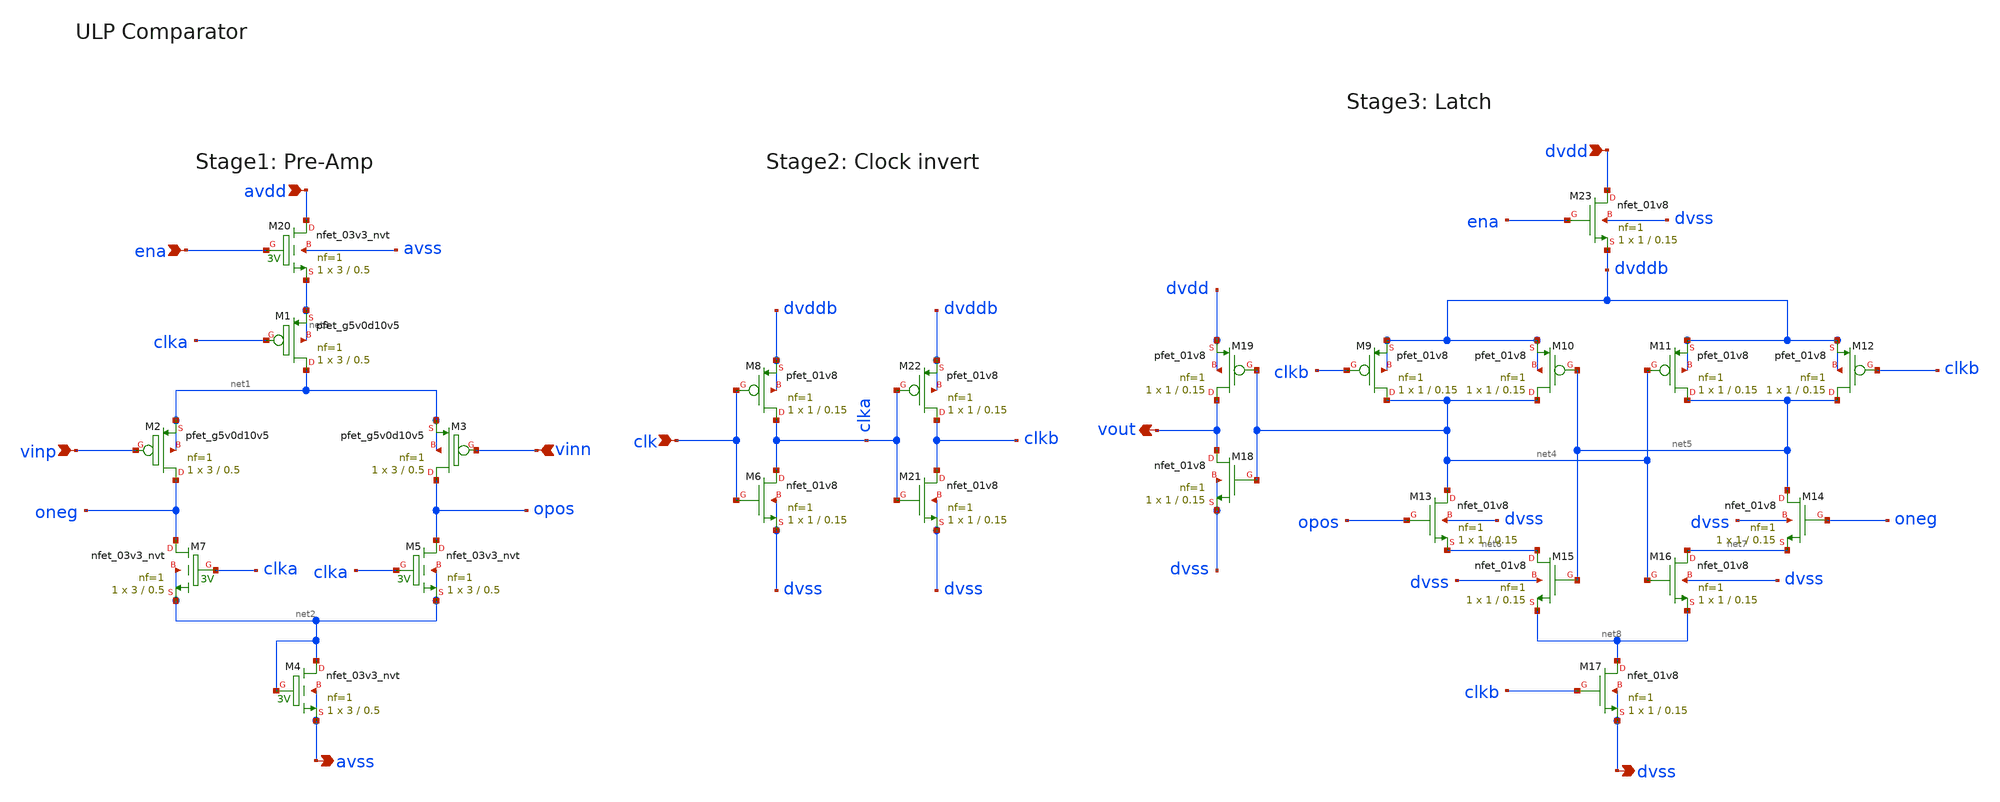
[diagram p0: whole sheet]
** sch_path: xschem/sky130_icrg_ip__ulpcomp2.sch
**.subckt sky130_icrg_ip__ulpcomp2 avdd vinp vinn avss vout dvss dvdd clk ena
*.ipin avdd
*.ipin vinp
*.ipin vinn
*.opin avss
*.opin vout
*.opin dvss
*.ipin dvdd
*.ipin clk
*.ipin ena
XM1 net1 clka net3 net3 sky130_fd_pr__pfet_g5v0d10v5 L=0.5 W=3 nf=1 ad='int((nf+1)/2) * W/nf * 0.29'
+ as='int((nf+2)/2) * W/nf * 0.29' pd='2*int((nf+1)/2) * (W/nf + 0.29)' ps='2*int((nf+2)/2) * (W/nf + 0.29)'
+ nrd='0.29 / W' nrs='0.29 / W' sa=0 sb=0 sd=0 mult=1 m=1
XM2 oneg vinp net1 net1 sky130_fd_pr__pfet_g5v0d10v5 L=0.5 W=3 nf=1 ad='int((nf+1)/2) * W/nf * 0.29'
+ as='int((nf+2)/2) * W/nf * 0.29' pd='2*int((nf+1)/2) * (W/nf + 0.29)' ps='2*int((nf+2)/2) * (W/nf + 0.29)'
+ nrd='0.29 / W' nrs='0.29 / W' sa=0 sb=0 sd=0 mult=1 m=1
XM3 opos vinn net1 net1 sky130_fd_pr__pfet_g5v0d10v5 L=0.5 W=3 nf=1 ad='int((nf+1)/2) * W/nf * 0.29'
+ as='int((nf+2)/2) * W/nf * 0.29' pd='2*int((nf+1)/2) * (W/nf + 0.29)' ps='2*int((nf+2)/2) * (W/nf + 0.29)'
+ nrd='0.29 / W' nrs='0.29 / W' sa=0 sb=0 sd=0 mult=1 m=1
XM7 oneg clka net2 net2 sky130_fd_pr__nfet_03v3_nvt L=0.5 W=3 nf=1 ad='int((nf+1)/2) * W/nf * 0.29' as='int((nf+2)/2) * W/nf * 0.29'
+ pd='2*int((nf+1)/2) * (W/nf + 0.29)' ps='2*int((nf+2)/2) * (W/nf + 0.29)' nrd='0.29 / W' nrs='0.29 / W'
+ sa=0 sb=0 sd=0 mult=1 m=1
XM5 opos clka net2 net2 sky130_fd_pr__nfet_03v3_nvt L=0.5 W=3 nf=1 ad='int((nf+1)/2) * W/nf * 0.29' as='int((nf+2)/2) * W/nf * 0.29'
+ pd='2*int((nf+1)/2) * (W/nf + 0.29)' ps='2*int((nf+2)/2) * (W/nf + 0.29)' nrd='0.29 / W' nrs='0.29 / W'
+ sa=0 sb=0 sd=0 mult=1 m=1
XM6 clka clk dvss dvss sky130_fd_pr__nfet_01v8 L=0.15 W=1 nf=1 ad='int((nf+1)/2) * W/nf * 0.29' as='int((nf+2)/2) * W/nf * 0.29'
+ pd='2*int((nf+1)/2) * (W/nf + 0.29)' ps='2*int((nf+2)/2) * (W/nf + 0.29)' nrd='0.29 / W' nrs='0.29 / W'
+ sa=0 sb=0 sd=0 mult=1 m=1
XM8 clka clk dvddb dvddb sky130_fd_pr__pfet_01v8 L=0.15 W=1 nf=1 ad='int((nf+1)/2) * W/nf * 0.29' as='int((nf+2)/2) * W/nf * 0.29'
+ pd='2*int((nf+1)/2) * (W/nf + 0.29)' ps='2*int((nf+2)/2) * (W/nf + 0.29)' nrd='0.29 / W' nrs='0.29 / W'
+ sa=0 sb=0 sd=0 mult=1 m=1
XM9 net4 clkb dvddb dvddb sky130_fd_pr__pfet_01v8 L=0.15 W=1 nf=1 ad='int((nf+1)/2) * W/nf * 0.29' as='int((nf+2)/2) * W/nf * 0.29'
+ pd='2*int((nf+1)/2) * (W/nf + 0.29)' ps='2*int((nf+2)/2) * (W/nf + 0.29)' nrd='0.29 / W' nrs='0.29 / W'
+ sa=0 sb=0 sd=0 mult=1 m=1
XM10 net4 net5 dvddb dvddb sky130_fd_pr__pfet_01v8 L=0.15 W=1 nf=1 ad='int((nf+1)/2) * W/nf * 0.29' as='int((nf+2)/2) * W/nf * 0.29'
+ pd='2*int((nf+1)/2) * (W/nf + 0.29)' ps='2*int((nf+2)/2) * (W/nf + 0.29)' nrd='0.29 / W' nrs='0.29 / W'
+ sa=0 sb=0 sd=0 mult=1 m=1
XM11 net5 net4 dvddb dvddb sky130_fd_pr__pfet_01v8 L=0.15 W=1 nf=1 ad='int((nf+1)/2) * W/nf * 0.29' as='int((nf+2)/2) * W/nf * 0.29'
+ pd='2*int((nf+1)/2) * (W/nf + 0.29)' ps='2*int((nf+2)/2) * (W/nf + 0.29)' nrd='0.29 / W' nrs='0.29 / W'
+ sa=0 sb=0 sd=0 mult=1 m=1
XM12 net5 clkb dvddb dvddb sky130_fd_pr__pfet_01v8 L=0.15 W=1 nf=1 ad='int((nf+1)/2) * W/nf * 0.29' as='int((nf+2)/2) * W/nf * 0.29'
+ pd='2*int((nf+1)/2) * (W/nf + 0.29)' ps='2*int((nf+2)/2) * (W/nf + 0.29)' nrd='0.29 / W' nrs='0.29 / W'
+ sa=0 sb=0 sd=0 mult=1 m=1
XM13 net4 opos net6 dvss sky130_fd_pr__nfet_01v8 L=0.15 W=1 nf=1 ad='int((nf+1)/2) * W/nf * 0.29' as='int((nf+2)/2) * W/nf * 0.29'
+ pd='2*int((nf+1)/2) * (W/nf + 0.29)' ps='2*int((nf+2)/2) * (W/nf + 0.29)' nrd='0.29 / W' nrs='0.29 / W'
+ sa=0 sb=0 sd=0 mult=1 m=1
XM14 net5 oneg net7 dvss sky130_fd_pr__nfet_01v8 L=0.15 W=1 nf=1 ad='int((nf+1)/2) * W/nf * 0.29' as='int((nf+2)/2) * W/nf * 0.29'
+ pd='2*int((nf+1)/2) * (W/nf + 0.29)' ps='2*int((nf+2)/2) * (W/nf + 0.29)' nrd='0.29 / W' nrs='0.29 / W'
+ sa=0 sb=0 sd=0 mult=1 m=1
XM15 net6 net5 net8 dvss sky130_fd_pr__nfet_01v8 L=0.15 W=1 nf=1 ad='int((nf+1)/2) * W/nf * 0.29' as='int((nf+2)/2) * W/nf * 0.29'
+ pd='2*int((nf+1)/2) * (W/nf + 0.29)' ps='2*int((nf+2)/2) * (W/nf + 0.29)' nrd='0.29 / W' nrs='0.29 / W'
+ sa=0 sb=0 sd=0 mult=1 m=1
XM16 net7 net4 net8 dvss sky130_fd_pr__nfet_01v8 L=0.15 W=1 nf=1 ad='int((nf+1)/2) * W/nf * 0.29' as='int((nf+2)/2) * W/nf * 0.29'
+ pd='2*int((nf+1)/2) * (W/nf + 0.29)' ps='2*int((nf+2)/2) * (W/nf + 0.29)' nrd='0.29 / W' nrs='0.29 / W'
+ sa=0 sb=0 sd=0 mult=1 m=1
XM17 net8 clkb dvss dvss sky130_fd_pr__nfet_01v8 L=0.15 W=1 nf=1 ad='int((nf+1)/2) * W/nf * 0.29' as='int((nf+2)/2) * W/nf * 0.29'
+ pd='2*int((nf+1)/2) * (W/nf + 0.29)' ps='2*int((nf+2)/2) * (W/nf + 0.29)' nrd='0.29 / W' nrs='0.29 / W'
+ sa=0 sb=0 sd=0 mult=1 m=1
XM4 net2 net2 avss avss sky130_fd_pr__nfet_03v3_nvt L=0.5 W=3 nf=1 ad='int((nf+1)/2) * W/nf * 0.29' as='int((nf+2)/2) * W/nf * 0.29'
+ pd='2*int((nf+1)/2) * (W/nf + 0.29)' ps='2*int((nf+2)/2) * (W/nf + 0.29)' nrd='0.29 / W' nrs='0.29 / W'
+ sa=0 sb=0 sd=0 mult=1 m=1
XM18 vout net4 dvss dvss sky130_fd_pr__nfet_01v8 L=0.15 W=1 nf=1 ad='int((nf+1)/2) * W/nf * 0.29' as='int((nf+2)/2) * W/nf * 0.29'
+ pd='2*int((nf+1)/2) * (W/nf + 0.29)' ps='2*int((nf+2)/2) * (W/nf + 0.29)' nrd='0.29 / W' nrs='0.29 / W'
+ sa=0 sb=0 sd=0 mult=1 m=1
XM19 vout net4 dvdd dvdd sky130_fd_pr__pfet_01v8 L=0.15 W=1 nf=1 ad='int((nf+1)/2) * W/nf * 0.29' as='int((nf+2)/2) * W/nf * 0.29'
+ pd='2*int((nf+1)/2) * (W/nf + 0.29)' ps='2*int((nf+2)/2) * (W/nf + 0.29)' nrd='0.29 / W' nrs='0.29 / W'
+ sa=0 sb=0 sd=0 mult=1 m=1
XM20 avdd ena net3 avss sky130_fd_pr__nfet_03v3_nvt L=0.5 W=3 nf=1 ad='int((nf+1)/2) * W/nf * 0.29' as='int((nf+2)/2) * W/nf * 0.29'
+ pd='2*int((nf+1)/2) * (W/nf + 0.29)' ps='2*int((nf+2)/2) * (W/nf + 0.29)' nrd='0.29 / W' nrs='0.29 / W'
+ sa=0 sb=0 sd=0 mult=1 m=1
XM23 dvdd ena dvddb dvss sky130_fd_pr__nfet_01v8 L=0.15 W=1 nf=1 ad='int((nf+1)/2) * W/nf * 0.29' as='int((nf+2)/2) * W/nf * 0.29'
+ pd='2*int((nf+1)/2) * (W/nf + 0.29)' ps='2*int((nf+2)/2) * (W/nf + 0.29)' nrd='0.29 / W' nrs='0.29 / W'
+ sa=0 sb=0 sd=0 mult=1 m=1
XM21 clkb clka dvss dvss sky130_fd_pr__nfet_01v8 L=0.15 W=1 nf=1 ad='int((nf+1)/2) * W/nf * 0.29' as='int((nf+2)/2) * W/nf * 0.29'
+ pd='2*int((nf+1)/2) * (W/nf + 0.29)' ps='2*int((nf+2)/2) * (W/nf + 0.29)' nrd='0.29 / W' nrs='0.29 / W'
+ sa=0 sb=0 sd=0 mult=1 m=1
XM22 clkb clka dvddb dvddb sky130_fd_pr__pfet_01v8 L=0.15 W=1 nf=1 ad='int((nf+1)/2) * W/nf * 0.29' as='int((nf+2)/2) * W/nf * 0.29'
+ pd='2*int((nf+1)/2) * (W/nf + 0.29)' ps='2*int((nf+2)/2) * (W/nf + 0.29)' nrd='0.29 / W' nrs='0.29 / W'
+ sa=0 sb=0 sd=0 mult=1 m=1
**.ends
.end
